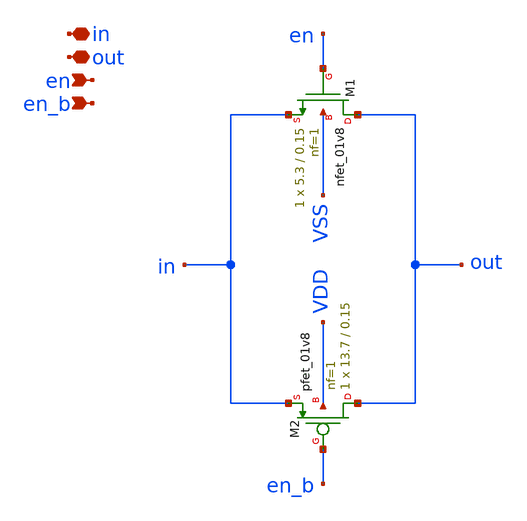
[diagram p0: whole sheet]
** sch_path: design/analog_modulator/schematic/transmission_gate_no_parameterized.sch
**.subckt transmission_gate_no_parameterized in out en en_b
*.iopin in
*.iopin out
*.ipin en
*.ipin en_b
XM1 out en in VSS sky130_fd_pr__nfet_01v8 L=0.15 W=5.3 nf=1 ad='int((nf+1)/2) * W/nf * 0.29' as='int((nf+2)/2) * W/nf * 0.29'
+ pd='2*int((nf+1)/2) * (W/nf + 0.29)' ps='2*int((nf+2)/2) * (W/nf + 0.29)' nrd='0.29 / W' nrs='0.29 / W'
+ sa=0 sb=0 sd=0 mult=1 m=1
XM2 out en_b in VDD sky130_fd_pr__pfet_01v8 L=0.15 W=13.7 nf=1 ad='int((nf+1)/2) * W/nf * 0.29' as='int((nf+2)/2) * W/nf * 0.29'
+ pd='2*int((nf+1)/2) * (W/nf + 0.29)' ps='2*int((nf+2)/2) * (W/nf + 0.29)' nrd='0.29 / W' nrs='0.29 / W'
+ sa=0 sb=0 sd=0 mult=1 m=1
**.ends
.end
